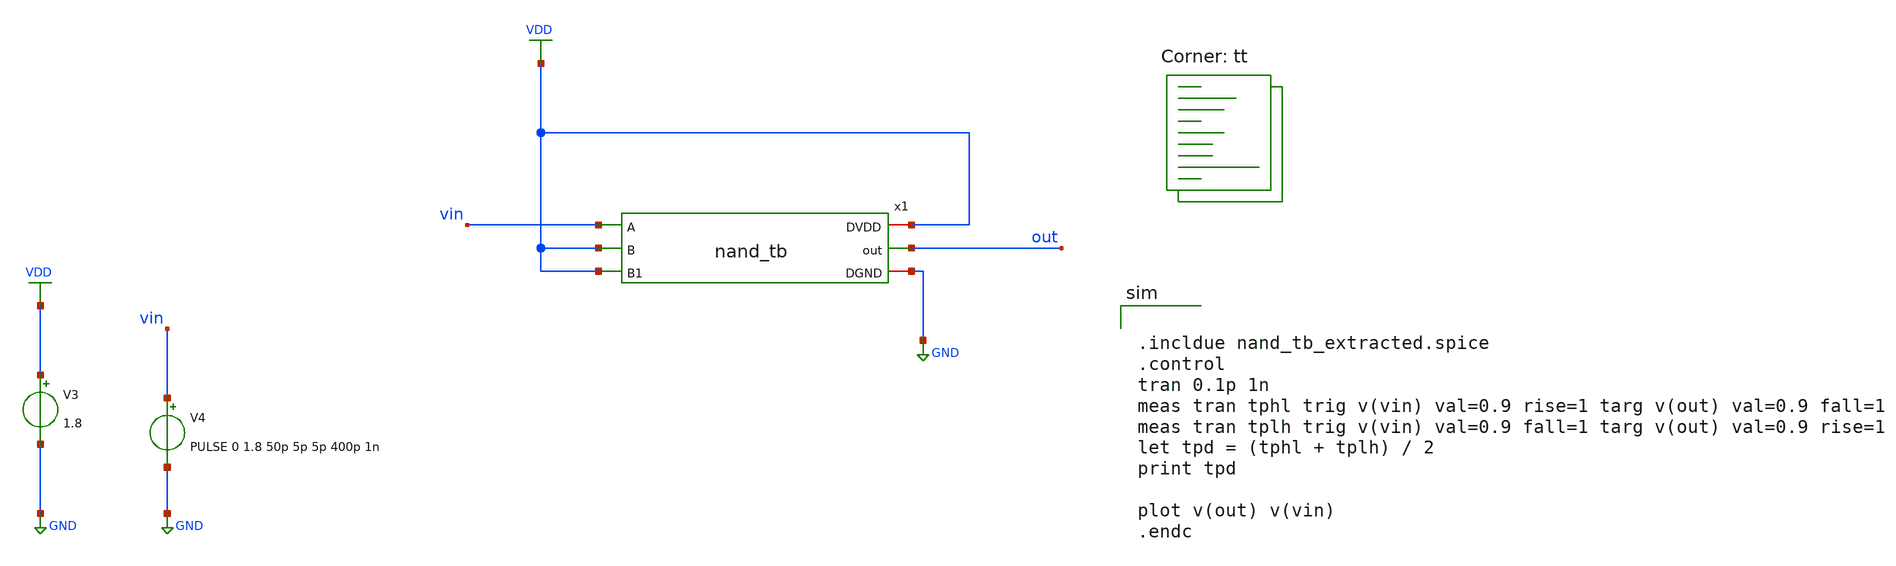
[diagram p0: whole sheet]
** sch_path: assignments/assignment5/assign2b.sch
**.subckt assign2b
x1 VDD vin out VDD VDD GND nand_tb
V3 VDD GND 1.8
V4 vin GND PULSE 0 1.8 50p 5p 5p 400p 1n
**** begin user architecture code
.lib $::SKYWATER_MODELS/sky130.lib.spice tt


.incldue nand_tb_extracted.spice
.control
tran 0.1p 1n
meas tran tphl trig v(vin) val=0.9 rise=1 targ v(out) val=0.9 fall=1
meas tran tplh trig v(vin) val=0.9 fall=1 targ v(out) val=0.9 rise=1
let tpd = (tphl + tplh) / 2
print tpd

plot v(out) v(vin)
.endc


**** end user architecture code
**.ends
.GLOBAL VDD
.GLOBAL GND
.end
